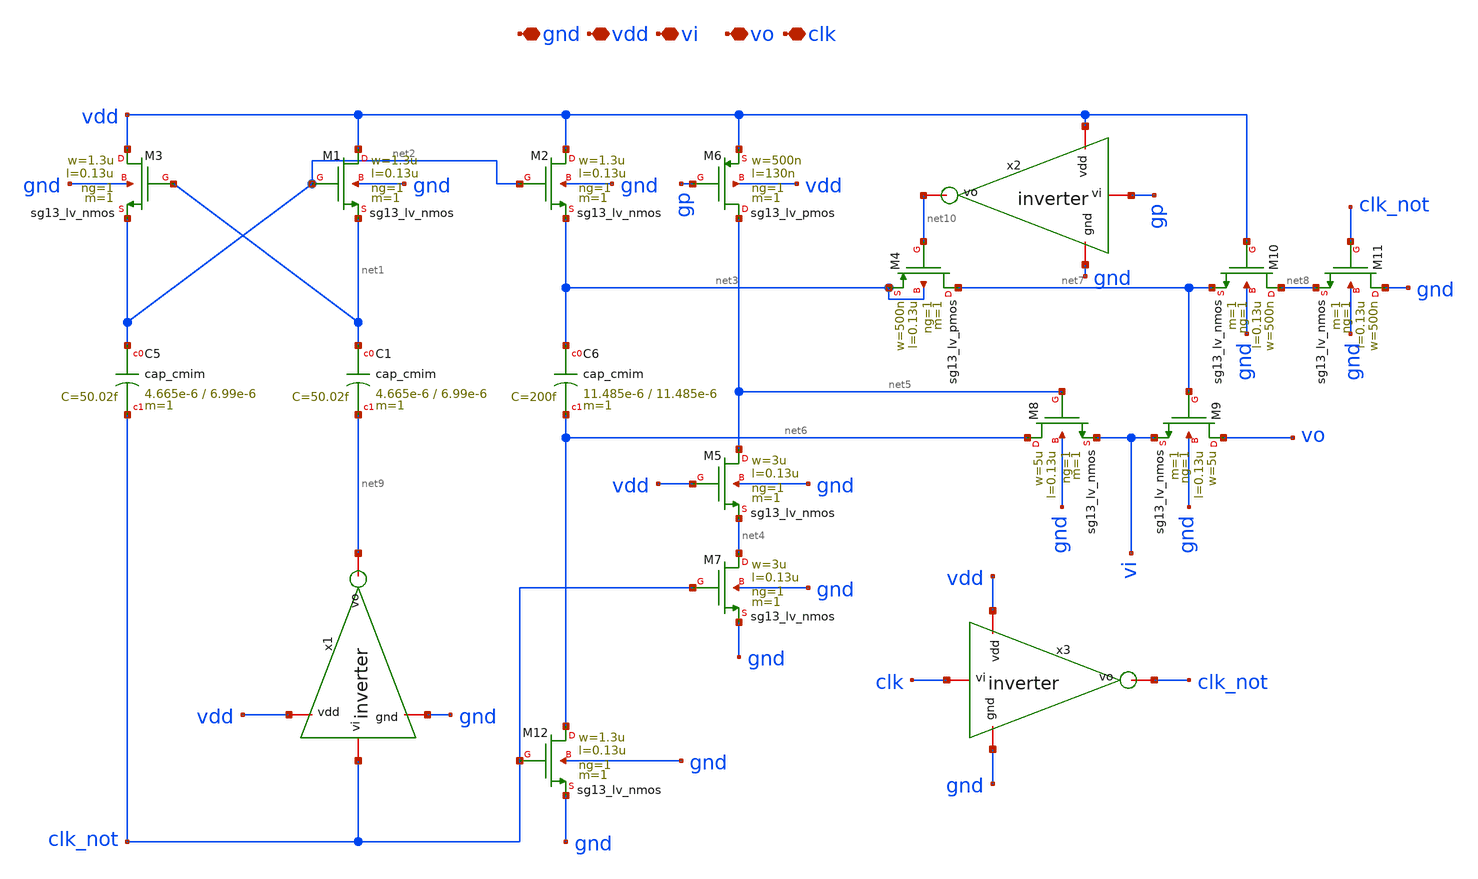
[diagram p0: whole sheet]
** sch_path: modules/module_3_8_bit_SAR_ADC/part_2_digital_comps/bootstrap_switch/schematic/bootstrap_switch.sch
**.subckt bootstrap_switch gnd vdd vi vo clk
*.iopin gnd
*.iopin vdd
*.iopin vi
*.iopin vo
*.iopin clk
XM1 vdd net2 net1 gnd sg13_lv_nmos w=1.3u l=0.13u ng=1 m=1 mm_ok=1
XM3 vdd net1 net2 gnd sg13_lv_nmos w=1.3u l=0.13u ng=1 m=1 mm_ok=1
XM4 net7 net10 net3 net3 sg13_lv_pmos w=500n l=0.13u ng=1 m=1 mm_ok=1
XM2 vdd net2 net3 gnd sg13_lv_nmos w=1.3u l=0.13u ng=1 m=1 mm_ok=1
XM6 net5 gp vdd vdd sg13_lv_pmos w=500n l=130n ng=1 m=1 mm_ok=1
XM5 net5 vdd net4 gnd sg13_lv_nmos w=3u l=0.13u ng=1 m=1 mm_ok=1
XM7 net4 clk_not gnd gnd sg13_lv_nmos w=3u l=0.13u ng=1 m=1 mm_ok=1
XC5 net2 clk_not cap_cmim w=4.665e-6 l=6.99e-6 m=1 mm_ok=1
XC6 net3 net6 cap_cmim w=11.485e-6 l=11.485e-6 m=1 mm_ok=1
XM8 net6 net5 vi gnd sg13_lv_nmos w=5u l=0.13u ng=1 m=1 mm_ok=1
XM9 vo net7 vi gnd sg13_lv_nmos w=5u l=0.13u ng=1 m=1 mm_ok=1
XM10 net8 vdd net7 gnd sg13_lv_nmos w=500n l=0.13u ng=1 m=1 mm_ok=1
XM11 gnd clk_not net8 gnd sg13_lv_nmos w=500n l=0.13u ng=1 m=1 mm_ok=1
XM12 net6 clk_not gnd gnd sg13_lv_nmos w=1.3u l=0.13u ng=1 m=1 mm_ok=1
XC1 net1 net9 cap_cmim w=4.665e-6 l=6.99e-6 m=1 mm_ok=1
x1 vdd clk_not net9 gnd inverter
x2 vdd gp net10 gnd inverter
x3 vdd clk clk_not gnd inverter
**.ends

* expanding   symbol:
*+  /home/pedersen/projects/IHP-AnalogAcademy/modules/module_3_8_bit_SAR_ADC/part_2_digital_comps/bootstrap_switch/schematic/inverter.sym # of pins=4
** sym_path: modules/module_3_8_bit_SAR_ADC/part_2_digital_comps/bootstrap_switch/schematic/inverter.sym
** sch_path: modules/module_3_8_bit_SAR_ADC/part_2_digital_comps/bootstrap_switch/schematic/inverter.sch
.subckt inverter vdd vi vo gnd
*.iopin vi
*.iopin vo
*.iopin gnd
*.iopin vdd
XM5 vo vi vdd vdd sg13_lv_pmos w=800n l=130n ng=1 m=1 mm_ok=1
XM7 vo vi gnd gnd sg13_lv_nmos w=400n l=130n ng=1 m=1 mm_ok=1
.ends

.end
